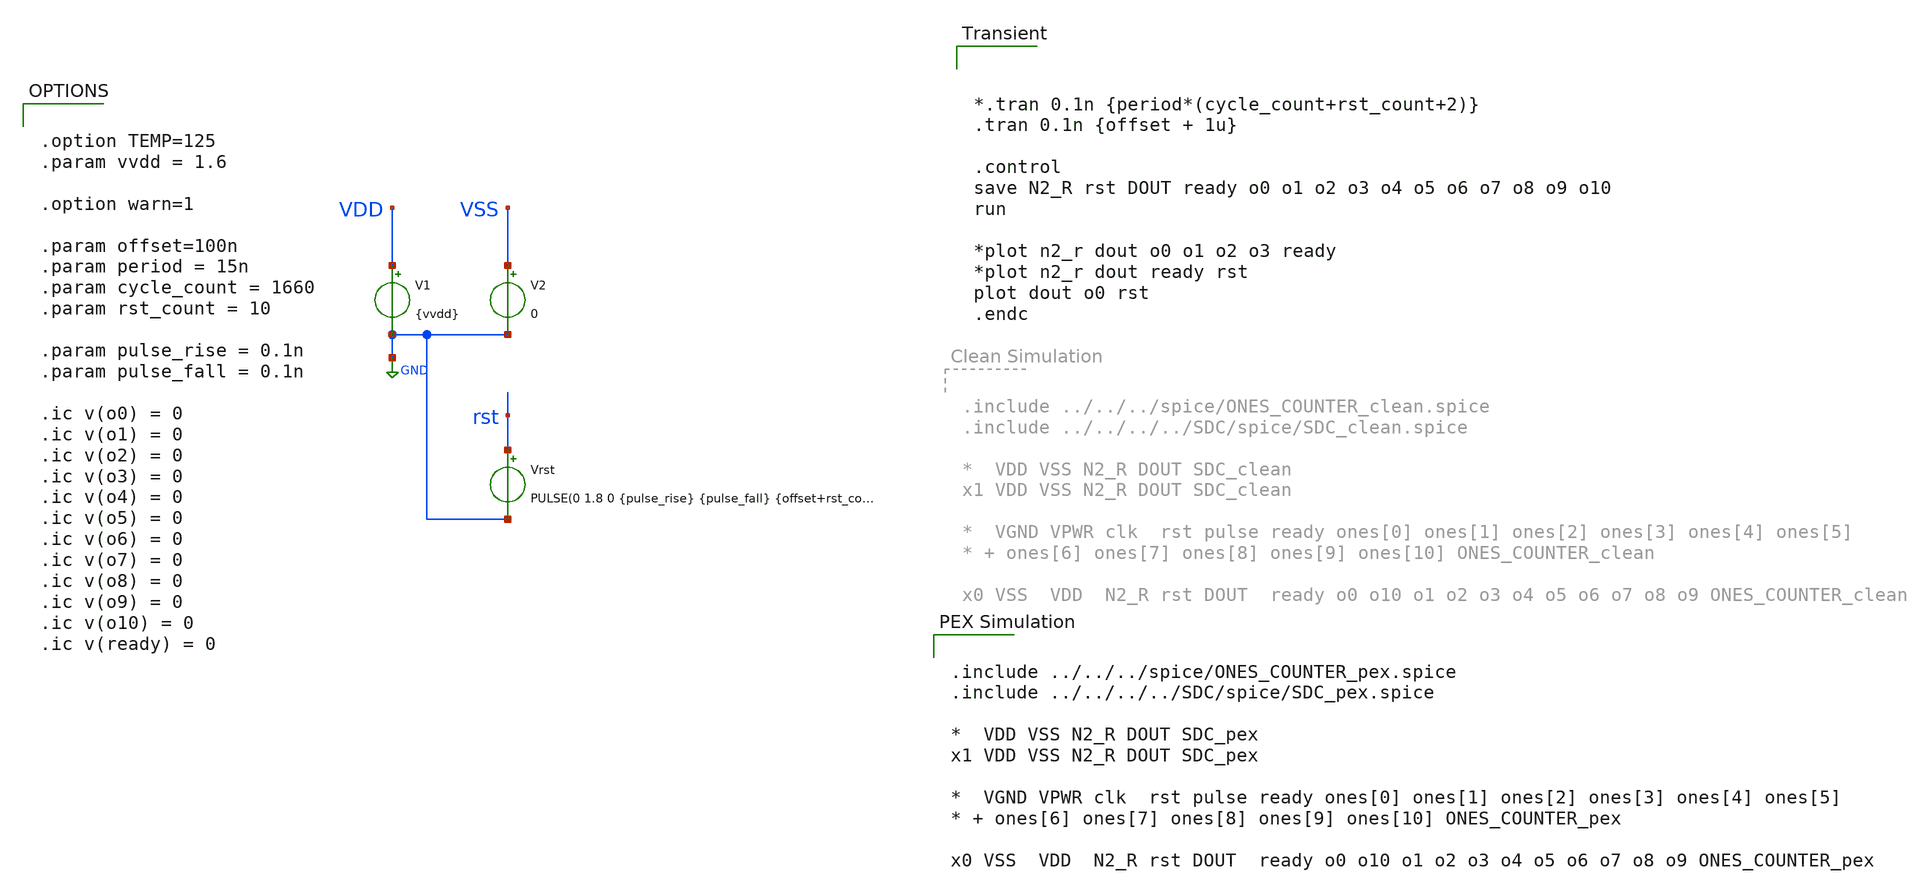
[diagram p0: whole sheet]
** sch_path: modules/ONES_COUNTER/test/dout_counter.sch
**.subckt dout_counter
V1 VDD GND {vvdd}
V2 VSS GND 0
Vrst rst GND PULSE(0 1.8 0 {pulse_rise} {pulse_fall} {offset+rst_count*period} {offset+rst_count*period}
+ 1)
**** begin user architecture code



*.tran 0.1n {period*(cycle_count+rst_count+2)}
.tran 0.1n {offset + 1u}

.control
save N2_R rst DOUT ready o0 o1 o2 o3 o4 o5 o6 o7 o8 o9 o10
run

*plot n2_r dout o0 o1 o2 o3 ready
*plot n2_r dout ready rst
plot dout o0 rst
.endc



.option TEMP=125
.param vvdd = 1.6

.option warn=1

.param offset=100n
.param period = 15n
.param cycle_count = 1660
.param rst_count = 10

.param pulse_rise = 0.1n
.param pulse_fall = 0.1n

.ic v(o0) = 0
.ic v(o1) = 0
.ic v(o2) = 0
.ic v(o3) = 0
.ic v(o4) = 0
.ic v(o5) = 0
.ic v(o6) = 0
.ic v(o7) = 0
.ic v(o8) = 0
.ic v(o9) = 0
.ic v(o10) = 0
.ic v(ready) = 0



.lib $env(PDK_ROOT)/$env(PDK)/libs.tech/combined/sky130.lib.spice ss
*.lib $env(PDK_ROOT)/$env(PDK)/libs.tech/ngspice/sky130.lib.spice ss

.include $env(PDK_ROOT)/$env(PDK)/libs.ref/sky130_fd_sc_hd/spice/sky130_fd_sc_hd.spice
*.include $env(PDK_ROOT)/$env(PDK)/libs.ref/sky130_fd_pr/spice/sky130_fd_pr__diode_pw2nd_05v5.model.spice



.include ../../../spice/ONES_COUNTER_pex.spice
.include ../../../../SDC/spice/SDC_pex.spice

*  VDD VSS N2_R DOUT SDC_pex
x1 VDD VSS N2_R DOUT SDC_pex

*  VGND VPWR clk  rst pulse ready ones[0] ones[1] ones[2] ones[3] ones[4] ones[5]
* + ones[6] ones[7] ones[8] ones[9] ones[10] ONES_COUNTER_pex

x0 VSS  VDD  N2_R rst DOUT  ready o0 o10 o1 o2 o3 o4 o5 o6 o7 o8 o9 ONES_COUNTER_pex


**** end user architecture code
**.ends
.GLOBAL GND
.end
